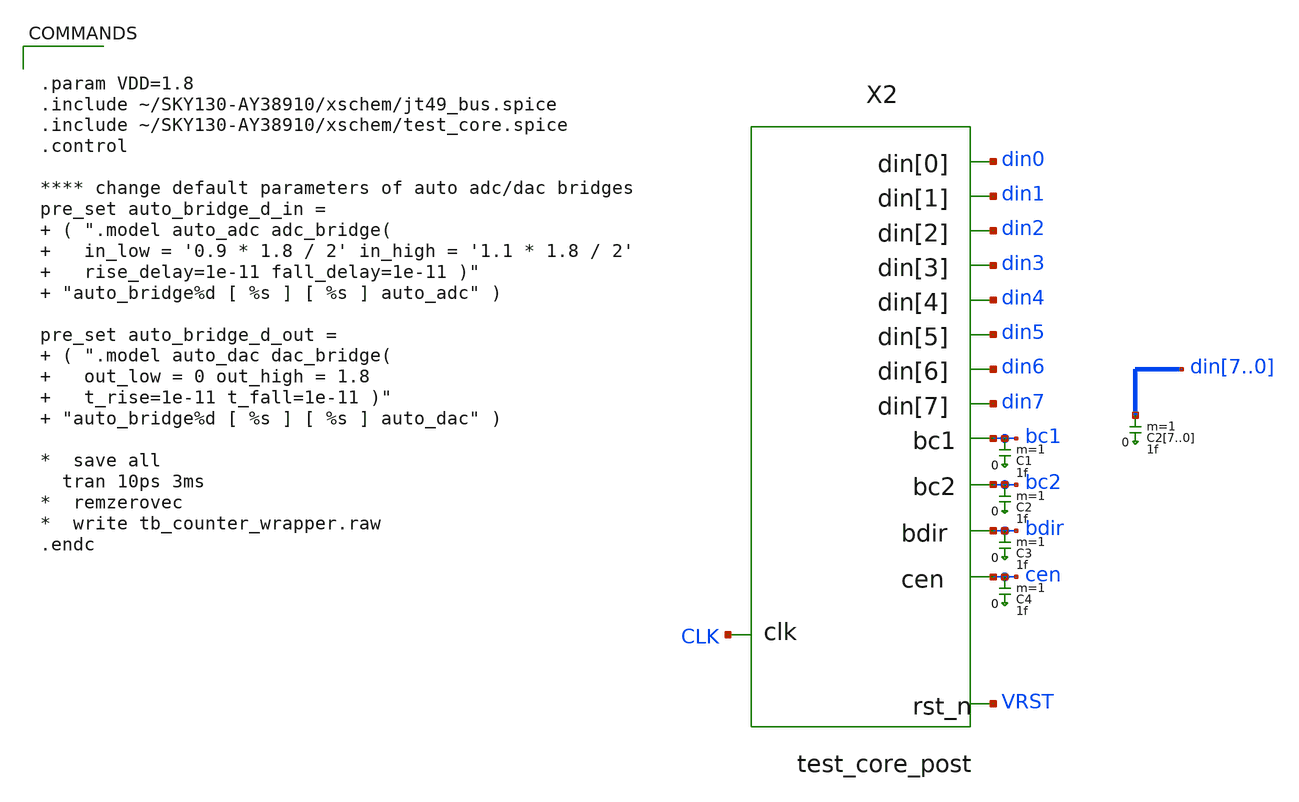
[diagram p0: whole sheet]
** sch_path: xschem/scratchpad.sch
**.subckt scratchpad
X2 CLK cen VRST bdir bc1 bc2 din7 din6 din5 din4 din3 din2 din1 din0 test_core
C27 din7 0 1f m=1
C26 din6 0 1f m=1
C25 din5 0 1f m=1
C24 din4 0 1f m=1
C23 din3 0 1f m=1
C22 din2 0 1f m=1
C21 din1 0 1f m=1
C20 din0 0 1f m=1
C1 bc1 0 1f m=1
C2 bc2 0 1f m=1
C3 bdir 0 1f m=1
C4 cen 0 1f m=1
**** begin user architecture code


.param VDD=1.8
.include ~/SKY130-AY38910/xschem/jt49_bus.spice
.include ~/SKY130-AY38910/xschem/test_core.spice
.control

**** change default parameters of auto adc/dac bridges
pre_set auto_bridge_d_in =  ( ".model auto_adc adc_bridge(    in_low = '0.9 * 1.8 / 2' in_high = '1.1 * 1.8 / 2'
+    rise_delay=1e-11 fall_delay=1e-11 )"  "auto_bridge%d [ %s ] [ %s ] auto_adc" )

pre_set auto_bridge_d_out =  ( ".model auto_dac dac_bridge(    out_low = 0 out_high = 1.8
+    t_rise=1e-11 t_fall=1e-11 )"  "auto_bridge%d [ %s ] [ %s ] auto_dac" )

*  save all
  tran 10ps 3ms
*  remzerovec
*  write tb_counter_wrapper.raw
.endc


**** end user architecture code
**.ends
.end
